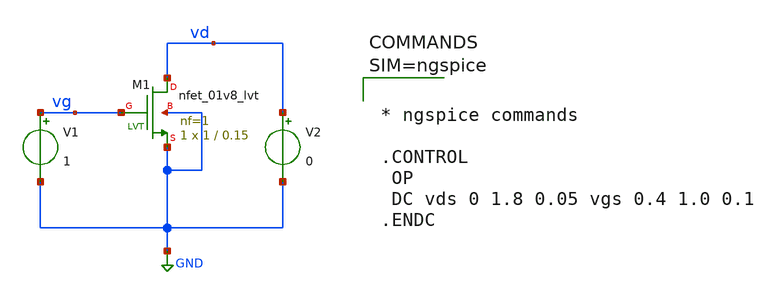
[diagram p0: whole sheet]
** sch_path: xschem/untitled-6.sch
**.subckt untitled-6
XM1 vd vg GND GND sky130_fd_pr__nfet_01v8_lvt L=0.15 W=1 nf=1 ad='int((1 + 1)/2) * 1 / 1 * 0.29' as='int((1 + 2)/2) * 1 / 1 * 0.29'
+ pd='2*int((1 + 1)/2) * (1 / 1 + 0.29)' ps='2*int((1 + 2)/2) * (1 / 1 + 0.29)' nrd='0.29 / 1 ' nrs='0.29 / 1 '
+ sa=0 sb=0 sd=0 mult=1 m=1
V1 vg GND 1
V2 vd GND 0
**** begin user architecture code



* ngspice commands

.CONTROL
 OP
 DC vds 0 1.8 0.05 vgs 0.4 1.0 0.1
.ENDC




** opencircuitdesign pdks install
.lib $::SKYWATER_MODELS/sky130.lib.spice tt

**** end user architecture code
**.ends
.GLOBAL GND
.end
